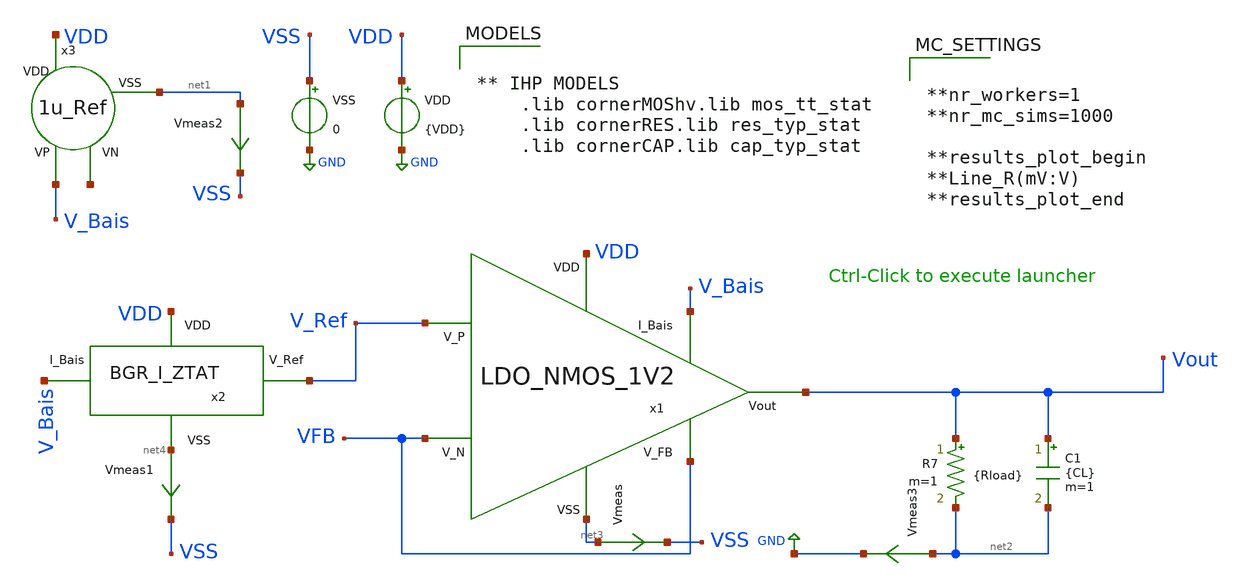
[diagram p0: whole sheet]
** sch_path: dependencies/PMU/PMU-main/testbenches/mc/xschem/PMU_DC_TB_MC_Line_R.sch
**.subckt PMU_DC_TB_MC_Line_R
VDD VDD GND {VDD}
Vmeas2 net1 VSS 0
.save i(vmeas2)
VSS VSS GND 0
C1 Vout net2 {CL} m=1
R7 Vout net2 {Rload} m=1
x1 VDD V_Bais V_Ref VFB Vout VFB net3 LDO_NMOS_1V2
Vmeas net3 VSS 0
.save i(vmeas)
Vmeas1 net4 VSS 0
.save i(vmeas1)
x2 VDD net4 V_Ref V_Bais BGR_I_ZTAT
x3 VDD V_Bais net5 net1 1u_Ref
Vmeas3 net2 GND 0
.save i(vmeas3)
**** begin user architecture code


** IHP MODELS
	.lib cornerMOShv.lib mos_tt_stat
	.lib cornerRES.lib res_typ_stat
	.lib cornerCAP.lib cap_typ_stat




.param mm_ok=1
.param mc_ok=1
.param temp=27
.options rshunt = 1e12
.options gmin=1e-12
.options reltol = 0.01 abstol = 1p
.option filetype=ascii
.save all
.param CL=100p
.param Rload=240k
.param VDD = 2.1
.control

dc VDD 2.1 3.3 0.05
meas dc V_Min MIN v(Vout)
meas dc V_Max MAX v(Vout)
let Line_R(mV:V)=(V_Max-V_Min)*1000/1.2

dc VDD 2.1 3.3 0.05
meas dc V_Min MIN v(Vout)
meas dc V_Max MAX v(Vout)
let Line_R(mV:V)=(V_Max-V_Min)*1000/1.2


echo results_save_begin
print Line_R(mV:V)
echo results_save_end

.endc




**nr_workers=1
**nr_mc_sims=1000

**results_plot_begin
**Line_R(mV:V)
**results_plot_end


**** end user architecture code
**.ends

* expanding   symbol:  LDO_NMOS_1V2.sym # of pins=7
** sym_path: dependencies/PMU/PMU-main/schematic/xschem/LDO_NMOS_1V2.sym
** sch_path: dependencies/PMU/PMU-main/schematic/xschem/LDO_NMOS_1V2.sch
.subckt LDO_NMOS_1V2 VDD I_Bais V_P V_N Vout V_FB VSS
*.iopin Vout
*.iopin VDD
*.iopin I_Bais
*.iopin V_P
*.iopin V_N
*.iopin V_FB
*.iopin VSS
Vmeas net6 VSS 0
.save i(vmeas)
XM6 VDD VG2 Vout GND sg13_hv_nmos w=10u l=0.45u ng=10 m=50 mm_ok=1
XR3 Vout V_FB sub! rhigh w=0.5e-6 l=18e-6 m=2 b=0 mm_ok=1
Vmeas1 net5 VSS 0
.save i(vmeas1)
XR2 V_FB net3 sub! rhigh w=0.5e-6 l=18e-6 m=2 b=0 mm_ok=1
XR4 net3 net2 sub! rhigh w=0.5e-6 l=18e-6 m=2 b=0 mm_ok=1
XR5 net2 net5 sub! rhigh w=0.5e-6 l=18e-6 m=2 b=0 mm_ok=1
x1 VDD I_Bais V_N V_P net1 VG2 net6 OpAmp_2etags
XC3 net4 net1 cap_cmim w=33.24e-6 l=50.0e-6 m=3 mm_ok=1
XC4 VG2 net5 cap_cmim w=33.24e-6 l=50e-6 m=2 mm_ok=1
XR1 VG2 net4 sub! rhigh w=0.5e-6 l=15e-6 m=1 b=0 mm_ok=1
.ends


* expanding   symbol:  /foss/designs/bgr/BGR_I_ZTAT.sym # of pins=4
** sym_path: dependencies/PMU/PMU-main/schematic/xschem/BGR_I_ZTAT.sym
** sch_path: dependencies/PMU/PMU-main/schematic/xschem/BGR_I_ZTAT.sch
.subckt BGR_I_ZTAT VDD VSS V_Ref I_Bais
*.iopin VDD
*.iopin I_Bais
*.iopin V_Ref
*.iopin VSS
XM7 net2 V_out VDD VDD sg13_hv_pmos w=1u l=3u ng=1 m=1 mm_ok=1
XM8 net3 V_out VDD VDD sg13_hv_pmos w=1u l=3u ng=1 m=1 mm_ok=1
XC1 VDD V_out cap_cmim w=13.265e-6 l=50e-6 m=1 mm_ok=1
Vmeas1 net3 Vp 0
.save i(vmeas1)
Vmeas22 Vn net1 0
.save i(vmeas22)
x2 VDD I_Bais Vp Vn V_out net5 Stage1
XM2 Vp1 Vp1 VSS VSS sg13_hv_nmos w=7.5u l=4u ng=1 m=2 mm_ok=1
XM3 net1 net1 VSS VSS sg13_hv_nmos w=7.5u l=4u ng=1 m=1 mm_ok=1
Vmeas2 net2 Vn 0
.save i(vmeas2)
Vmeas5 net4 Vp1 0
.save i(vmeas5)
Vmeas6 net5 VSS 0
.save i(vmeas6)
XM1 V_Ref V_out VDD VDD sg13_hv_pmos w=1u l=3u ng=1 m=1 mm_ok=1
Vmeas3 V_Ref net11 0
.save i(vmeas3)
XM4 net11 net11 VSS VSS sg13_hv_nmos w=2u l=2.75u ng=1 m=1 mm_ok=1
XM6 net8 Vn VSS GND sg13_hv_nmos w=4u l=2u ng=1 m=1 mm_ok=1
XM5 net6 net6 VDD VDD sg13_hv_pmos w=4u l=1u ng=1 m=1 mm_ok=1
XM9 net7 net6 VDD VDD sg13_hv_pmos w=4u l=1u ng=1 m=1 mm_ok=1
Vmeas4 net7 net8 0
.save i(vmeas4)
XC3 net9 VSS cap_cmim w=5e-6 l=5e-6 m=1 mm_ok=1
XM10 VSS VDD net6 VDD sg13_hv_pmos w=4u l=1u ng=1 m=1 mm_ok=1
XMSU V_out net8 net10 net10 sg13_hv_nmos w=4u l=2u ng=1 m=1 mm_ok=1
Vmeas8 net6 net9 0
.save i(vmeas8)
Vmeas9 net10 VSS 0
.save i(vmeas9)
XR4 Vp VSS sub! rhigh w=0.5e-6 l=80e-6 m=1 b=0 mm_ok=1
XR5 Vp net4 sub! rhigh w=0.5e-6 l=210e-6 m=1 b=0 mm_ok=1
.ends


* expanding   symbol:  1u_Ref.sym # of pins=4
** sym_path: dependencies/PMU/PMU-main/schematic/xschem/1u_Ref.sym
** sch_path: dependencies/PMU/PMU-main/schematic/xschem/1u_Ref.sch
.subckt 1u_Ref VDD VP VN VSS
*.iopin VDD
*.iopin VSS
*.iopin VP
*.iopin VN
XM1 VP VP VDD VDD sg13_hv_pmos w=10u l=2u ng=1 m=1 mm_ok=1
XM2 VN VP VDD VDD sg13_hv_pmos w=10u l=2u ng=1 m=1 mm_ok=1
XM6 net1 net1 VDD VDD sg13_hv_pmos w=0.3u l=10u ng=1 m=1 mm_ok=1
XM7 V1 VN net4 net4 sg13_hv_nmos w=1u l=6u ng=1 m=1 mm_ok=1
XM5 net3 V1 VN VSS sg13_hv_nmos w=1u l=10u ng=1 m=1 mm_ok=1
Vmeas2 net2 VSS 0
.save i(vmeas2)
XM4 VN VR net2 net2 sg13_hv_nmos w=10u l=1u ng=1 m=1 mm_ok=1
XM3 net5 VN VR VSS sg13_hv_nmos w=10u l=1u ng=1 m=4 mm_ok=1
Vmeas1 VP net5 0
.save i(vmeas1)
Vmeas3 VP net3 0
.save i(vmeas3)
Vmeas4 net4 VSS 0
.save i(vmeas4)
XM8 V1 V1 net1 VDD sg13_hv_pmos w=0.3u l=10u ng=1 m=1 mm_ok=1
XR1 VR VSS sub! rhigh w=0.5e-6 l=185e-6 m=1 b=0 mm_ok=1
.ends


* expanding   symbol:  OpAmp_2etags.sym # of pins=7
** sym_path: dependencies/PMU/PMU-main/schematic/xschem/OpAmp_2etags.sym
** sch_path: dependencies/PMU/PMU-main/schematic/xschem/OpAmp_2etags.sch
.subckt OpAmp_2etags VDD I_Bais VP VN VG VOUT VSS
*.iopin VDD
*.iopin I_Bais
*.iopin VP
*.iopin VN
*.iopin VG
*.iopin VOUT
*.iopin VSS
XM3 VX2 VX2 VSS VSS sg13_hv_nmos w=10u l=2u ng=1 m=2 mm_ok=1
XM1 VX2 VP net1 VDD sg13_hv_pmos w=5u l=2u ng=1 m=2 mm_ok=1
XM2 VG VN net1 VDD sg13_hv_pmos w=5u l=2u ng=1 m=2 mm_ok=1
XM4 VG VX2 VSS VSS sg13_hv_nmos w=10u l=2u ng=1 m=2 mm_ok=1
XM5 net1 I_Bais VDD VDD sg13_hv_pmos w=10u l=2u ng=1 m=4 mm_ok=1
XM7 VOUT I_Bais VDD VDD sg13_hv_pmos w=10u l=2u ng=1 m=8 mm_ok=1
XM6 VOUT VG VSS VSS sg13_hv_nmos w=10u l=2u ng=1 m=8 mm_ok=1
.ends


* expanding   symbol:  Stage1.sym # of pins=6
** sym_path: dependencies/PMU/PMU-main/schematic/xschem/Stage1.sym
** sch_path: dependencies/PMU/PMU-main/schematic/xschem/Stage1.sch
.subckt Stage1 VDD VB Vin1 Vin2 Vout1 VSS
*.iopin VDD
*.ipin VB
*.ipin Vin1
*.ipin Vin2
*.iopin VSS
*.opin Vout1
XM1 net1 Vin1 VX VDD sg13_hv_pmos w=10u l=5u ng=2 m=2 mm_ok=1
XM2 net1 net1 VSS VSS sg13_hv_nmos w=1u l=10u ng=2 m=2 mm_ok=1
XM3 Vout1 net1 VSS VSS sg13_hv_nmos w=1u l=10u ng=2 m=2 mm_ok=1
XM4 Vout1 Vin2 VX VDD sg13_hv_pmos w=10u l=5u ng=2 m=2 mm_ok=1
XM5 VX VB VDD VDD sg13_hv_pmos w=10u l=2u ng=1 m=5 mm_ok=1
.ends

.GLOBAL GND
.end
